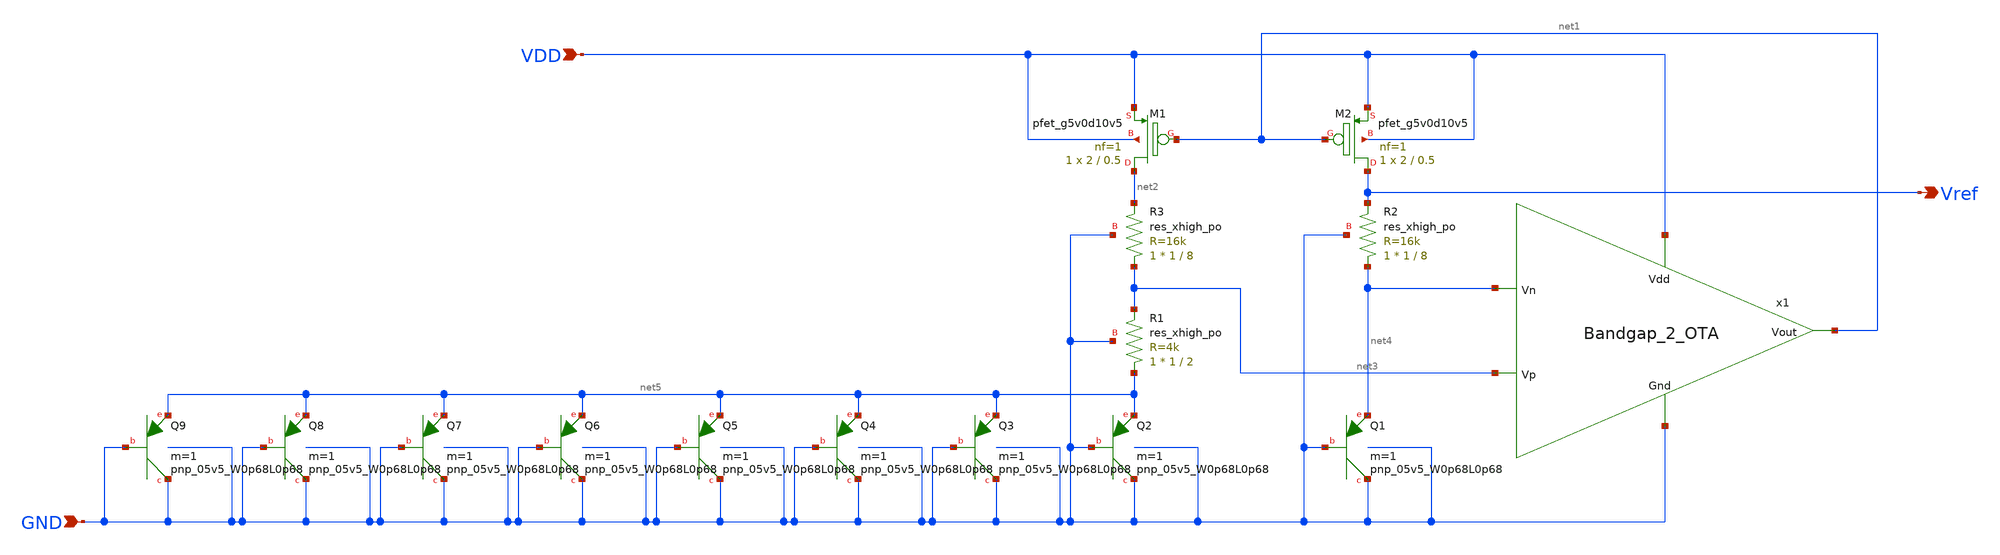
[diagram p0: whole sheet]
** sch_path: Analog_Blocks/Bandgap/Schematics/BGR_2/Bandgap_2.sch
**.subckt Bandgap_2 VDD GND Vref
*.ipin VDD
*.ipin GND
*.opin Vref
XM1 net2 net1 VDD VDD sky130_fd_pr__pfet_g5v0d10v5 L=0.5 W=2 nf=1 ad='int((nf+1)/2) * W/nf * 0.29' as='int((nf+2)/2) * W/nf * 0.29'
+ pd='2*int((nf+1)/2) * (W/nf + 0.29)' ps='2*int((nf+2)/2) * (W/nf + 0.29)' nrd='0.29 / W' nrs='0.29 / W'
+ sa=0 sb=0 sd=0 mult=1 m=1
XM2 Vref net1 VDD VDD sky130_fd_pr__pfet_g5v0d10v5 L=0.5 W=2 nf=1 ad='int((nf+1)/2) * W/nf * 0.29' as='int((nf+2)/2) * W/nf * 0.29'
+ pd='2*int((nf+1)/2) * (W/nf + 0.29)' ps='2*int((nf+2)/2) * (W/nf + 0.29)' nrd='0.29 / W' nrs='0.29 / W'
+ sa=0 sb=0 sd=0 mult=1 m=1
XR1 net5 net3 GND sky130_fd_pr__res_xhigh_po W=1 L=2 mult=1 m=1
XR2 net4 Vref GND sky130_fd_pr__res_xhigh_po W=1 L=8 mult=1 m=1
XR3 net3 net2 GND sky130_fd_pr__res_xhigh_po W=1 L=8 mult=1 m=1
XQ1 GND GND net4 sky130_fd_pr__pnp_05v5_W0p68L0p68 m=1
XQ2 GND GND net5 sky130_fd_pr__pnp_05v5_W0p68L0p68 m=1
XQ3 GND GND net5 sky130_fd_pr__pnp_05v5_W0p68L0p68 m=1
XQ4 GND GND net5 sky130_fd_pr__pnp_05v5_W0p68L0p68 m=1
XQ5 GND GND net5 sky130_fd_pr__pnp_05v5_W0p68L0p68 m=1
XQ6 GND GND net5 sky130_fd_pr__pnp_05v5_W0p68L0p68 m=1
XQ7 GND GND net5 sky130_fd_pr__pnp_05v5_W0p68L0p68 m=1
XQ8 GND GND net5 sky130_fd_pr__pnp_05v5_W0p68L0p68 m=1
XQ9 GND GND net5 sky130_fd_pr__pnp_05v5_W0p68L0p68 m=1
x1 VDD net1 net4 net3 GND Bandgap_2_OTA
**.ends

* expanding   symbol:
*+  /home/eslam/Analog_Design/Analog_Blocks/Bandgap/Schematics/BGR_2/Bandgap_2_OTA.sym # of pins=5
** sym_path: Analog_Blocks/Bandgap/Schematics/BGR_2/Bandgap_2_OTA.sym
** sch_path: Analog_Blocks/Bandgap/Schematics/BGR_2/Bandgap_2_OTA.sch
.subckt Bandgap_2_OTA Vdd Vout Vn Vp Gnd
*.ipin Vdd
*.ipin Gnd
*.ipin Vn
*.ipin Vp
*.opin Vout
XM5 net3 net4 Vdd Vdd sky130_fd_pr__pfet_g5v0d10v5 L=1 W=10 nf=1 ad='int((nf+1)/2) * W/nf * 0.29' as='int((nf+2)/2) * W/nf * 0.29'
+ pd='2*int((nf+1)/2) * (W/nf + 0.29)' ps='2*int((nf+2)/2) * (W/nf + 0.29)' nrd='0.29 / W' nrs='0.29 / W'
+ sa=0 sb=0 sd=0 mult=1 m=1
XM7 Vout net4 Vdd Vdd sky130_fd_pr__pfet_g5v0d10v5 L=1 W=54 nf=1 ad='int((nf+1)/2) * W/nf * 0.29' as='int((nf+2)/2) * W/nf * 0.29'
+ pd='2*int((nf+1)/2) * (W/nf + 0.29)' ps='2*int((nf+2)/2) * (W/nf + 0.29)' nrd='0.29 / W' nrs='0.29 / W'
+ sa=0 sb=0 sd=0 mult=1 m=1
XM2 net1 Vp net3 Vdd sky130_fd_pr__pfet_g5v0d10v5 L=1 W=30 nf=1 ad='int((nf+1)/2) * W/nf * 0.29' as='int((nf+2)/2) * W/nf * 0.29'
+ pd='2*int((nf+1)/2) * (W/nf + 0.29)' ps='2*int((nf+2)/2) * (W/nf + 0.29)' nrd='0.29 / W' nrs='0.29 / W'
+ sa=0 sb=0 sd=0 mult=1 m=1
XM1 net2 Vn net3 Vdd sky130_fd_pr__pfet_g5v0d10v5 L=1 W=30 nf=1 ad='int((nf+1)/2) * W/nf * 0.29' as='int((nf+2)/2) * W/nf * 0.29'
+ pd='2*int((nf+1)/2) * (W/nf + 0.29)' ps='2*int((nf+2)/2) * (W/nf + 0.29)' nrd='0.29 / W' nrs='0.29 / W'
+ sa=0 sb=0 sd=0 mult=1 m=1
XM8 Vout net1 Gnd Gnd sky130_fd_pr__nfet_g5v0d10v5 L=0.5 W=75 nf=1 ad='int((nf+1)/2) * W/nf * 0.29' as='int((nf+2)/2) * W/nf * 0.29'
+ pd='2*int((nf+1)/2) * (W/nf + 0.29)' ps='2*int((nf+2)/2) * (W/nf + 0.29)' nrd='0.29 / W' nrs='0.29 / W'
+ sa=0 sb=0 sd=0 mult=1 m=1
XM4 net1 net2 Gnd Gnd sky130_fd_pr__nfet_g5v0d10v5 L=0.5 W=7.5 nf=1 ad='int((nf+1)/2) * W/nf * 0.29'
+ as='int((nf+2)/2) * W/nf * 0.29' pd='2*int((nf+1)/2) * (W/nf + 0.29)' ps='2*int((nf+2)/2) * (W/nf + 0.29)'
+ nrd='0.29 / W' nrs='0.29 / W' sa=0 sb=0 sd=0 mult=1 m=1
XM3 net2 net2 Gnd Gnd sky130_fd_pr__nfet_g5v0d10v5 L=0.5 W=7.5 nf=1 ad='int((nf+1)/2) * W/nf * 0.29'
+ as='int((nf+2)/2) * W/nf * 0.29' pd='2*int((nf+1)/2) * (W/nf + 0.29)' ps='2*int((nf+2)/2) * (W/nf + 0.29)'
+ nrd='0.29 / W' nrs='0.29 / W' sa=0 sb=0 sd=0 mult=1 m=1
XC1 net1 Vout sky130_fd_pr__cap_mim_m3_2 W=2 L=1 MF=1 m=1
XM6 net5 net4 Vdd Vdd sky130_fd_pr__pfet_g5v0d10v5 L=2 W=30 nf=1 ad='int((nf+1)/2) * W/nf * 0.29' as='int((nf+2)/2) * W/nf * 0.29'
+ pd='2*int((nf+1)/2) * (W/nf + 0.29)' ps='2*int((nf+2)/2) * (W/nf + 0.29)' nrd='0.29 / W' nrs='0.29 / W'
+ sa=0 sb=0 sd=0 mult=1 m=1
XM9 net4 net4 Vdd Vdd sky130_fd_pr__pfet_g5v0d10v5 L=2 W=30 nf=1 ad='int((nf+1)/2) * W/nf * 0.29' as='int((nf+2)/2) * W/nf * 0.29'
+ pd='2*int((nf+1)/2) * (W/nf + 0.29)' ps='2*int((nf+2)/2) * (W/nf + 0.29)' nrd='0.29 / W' nrs='0.29 / W'
+ sa=0 sb=0 sd=0 mult=1 m=1
XM10 net4 net5 net6 Gnd sky130_fd_pr__nfet_g5v0d10v5 L=5 W=15 nf=1 ad='int((nf+1)/2) * W/nf * 0.29' as='int((nf+2)/2) * W/nf * 0.29'
+ pd='2*int((nf+1)/2) * (W/nf + 0.29)' ps='2*int((nf+2)/2) * (W/nf + 0.29)' nrd='0.29 / W' nrs='0.29 / W'
+ sa=0 sb=0 sd=0 mult=1 m=1
XM11 net5 net5 Gnd Gnd sky130_fd_pr__nfet_g5v0d10v5 L=5 W=5 nf=1 ad='int((nf+1)/2) * W/nf * 0.29' as='int((nf+2)/2) * W/nf * 0.29'
+ pd='2*int((nf+1)/2) * (W/nf + 0.29)' ps='2*int((nf+2)/2) * (W/nf + 0.29)' nrd='0.29 / W' nrs='0.29 / W'
+ sa=0 sb=0 sd=0 mult=1 m=1
XR1 Gnd net6 Gnd sky130_fd_pr__res_xhigh_po W=1 L=3.7 mult=1 m=1
.ends

.end
